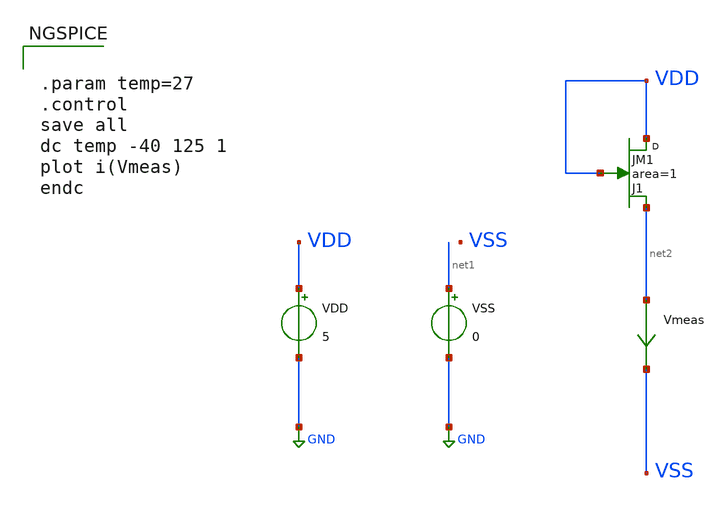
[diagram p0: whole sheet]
** sch_path: Learning/single_ended_amplifiers/A_High_Precision_Micropower_Operational_Amplifier_custom_models/current_reference/testbench.sch
**.subckt testbench
VDD VDD GND 5
VSS net1 GND 0
J1 VDD VDD net2 JM1 area=1 m=1
Vmeas net2 VSS 0
.save i(vmeas)
**** begin user architecture code


.param temp=27
.control
save all
dc temp -40 125 1
plot i(Vmeas)
endc



.model JM1 NJF (VTO=-2.0 BETA=1.0E-4 LAMBDA=0.02 RD=10 RS=5 CGS=5pF CGD=3pF PB=0.7 IS=1E-14 FC=0.5)


**** end user architecture code
**.ends
.GLOBAL GND
.end
